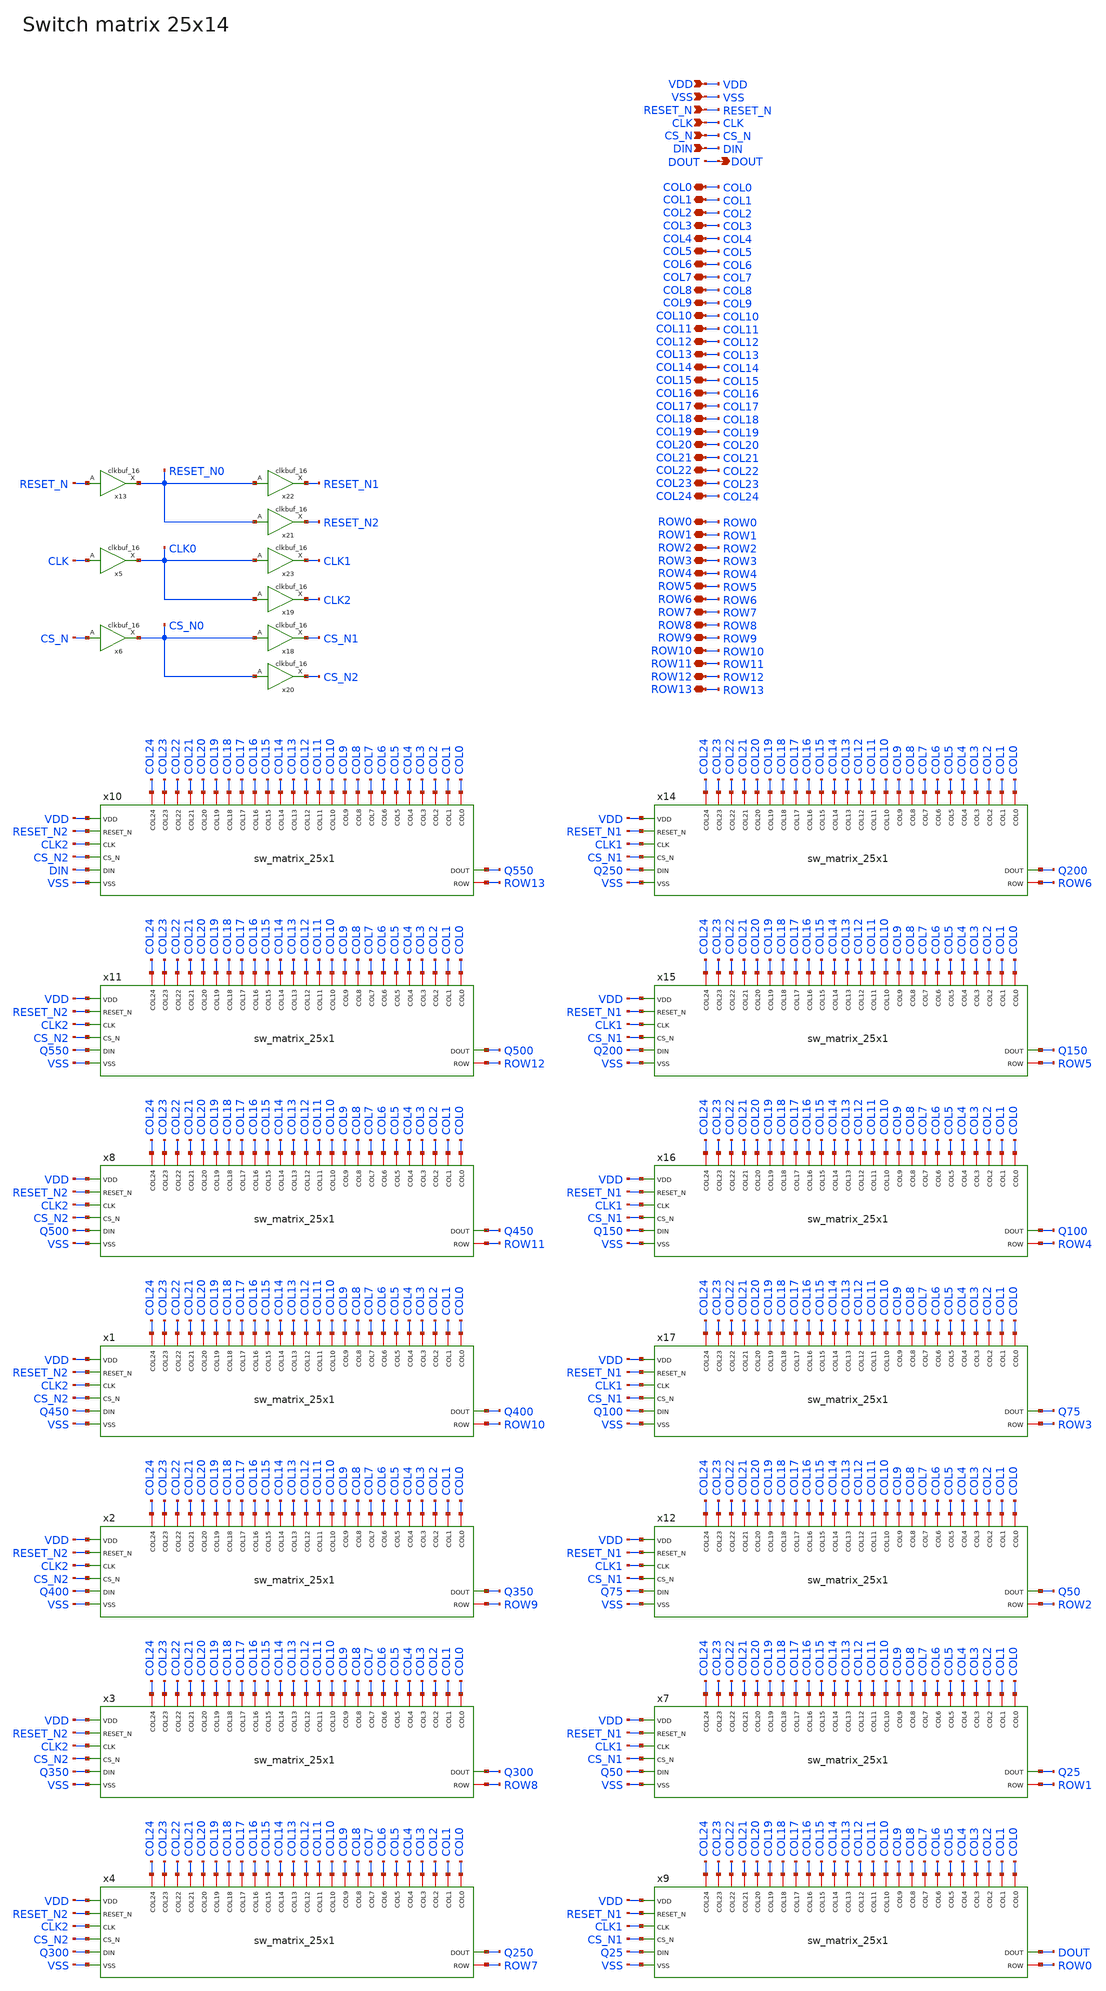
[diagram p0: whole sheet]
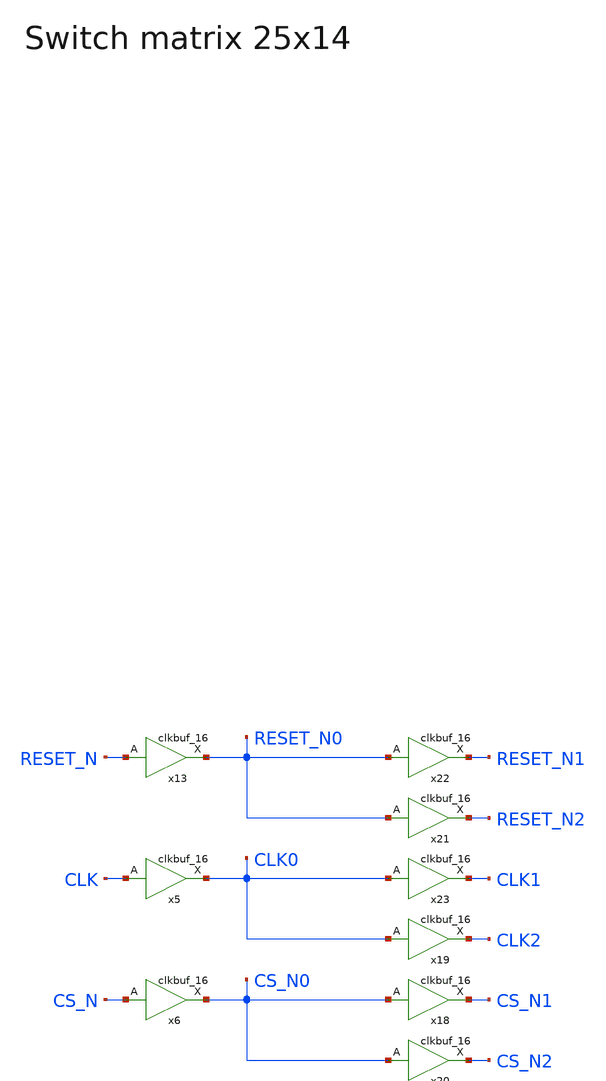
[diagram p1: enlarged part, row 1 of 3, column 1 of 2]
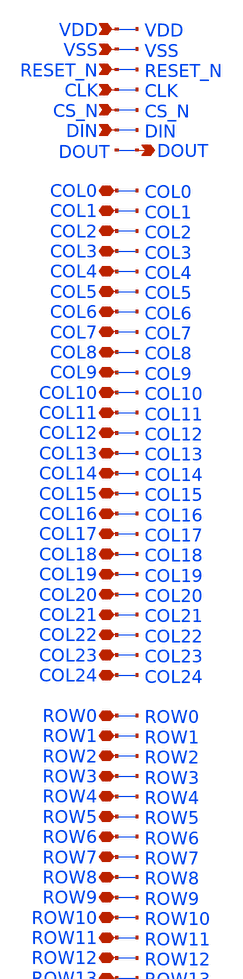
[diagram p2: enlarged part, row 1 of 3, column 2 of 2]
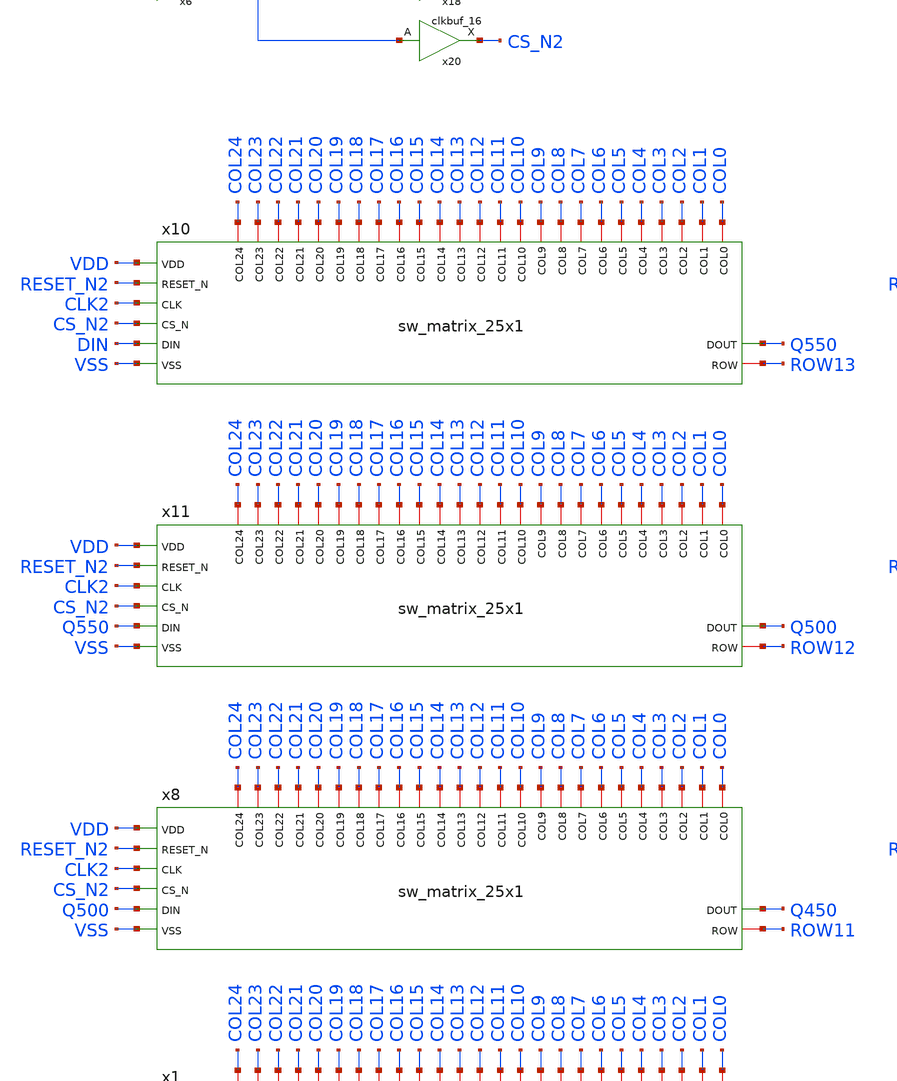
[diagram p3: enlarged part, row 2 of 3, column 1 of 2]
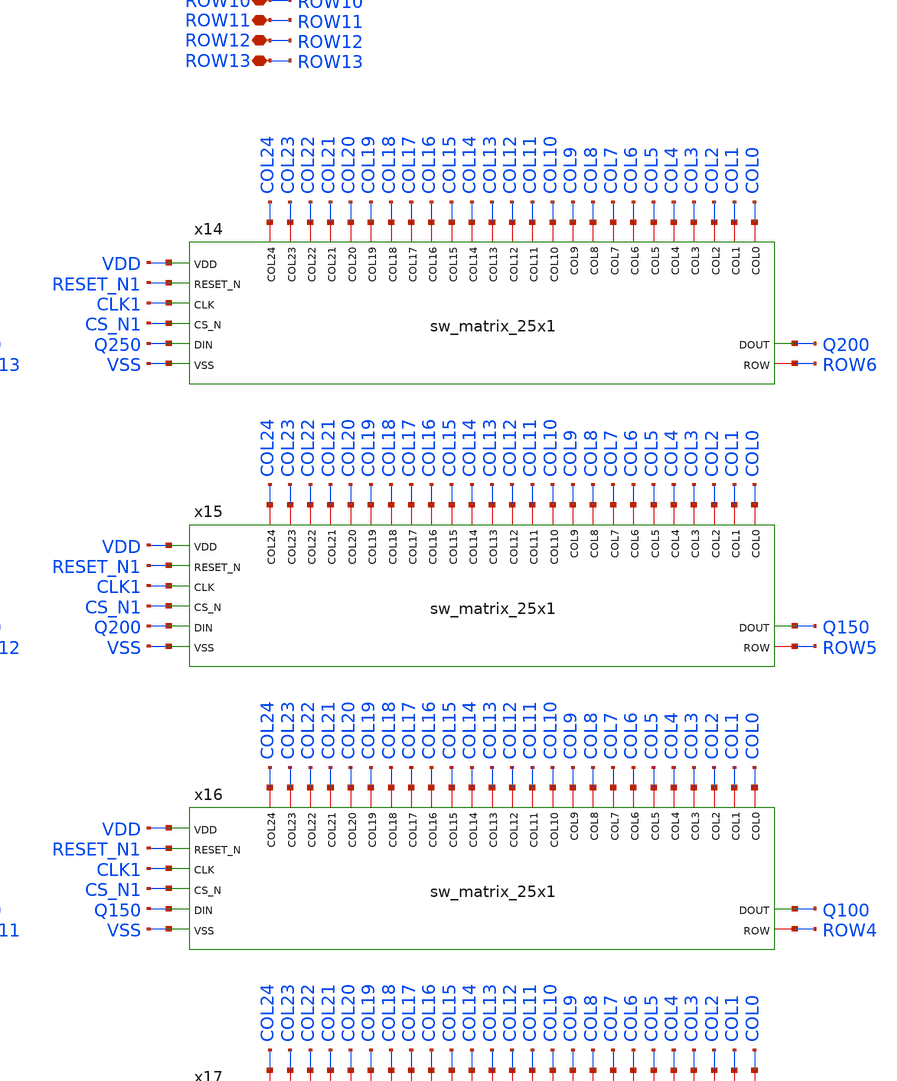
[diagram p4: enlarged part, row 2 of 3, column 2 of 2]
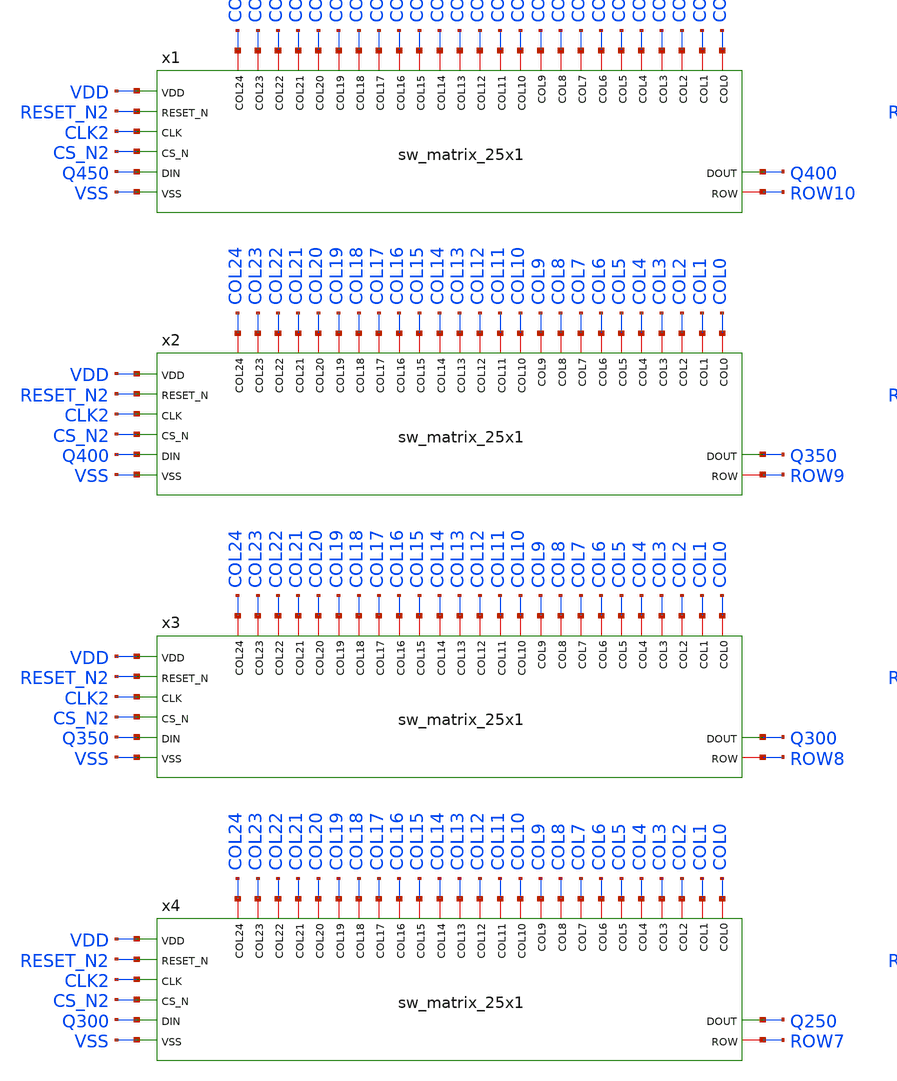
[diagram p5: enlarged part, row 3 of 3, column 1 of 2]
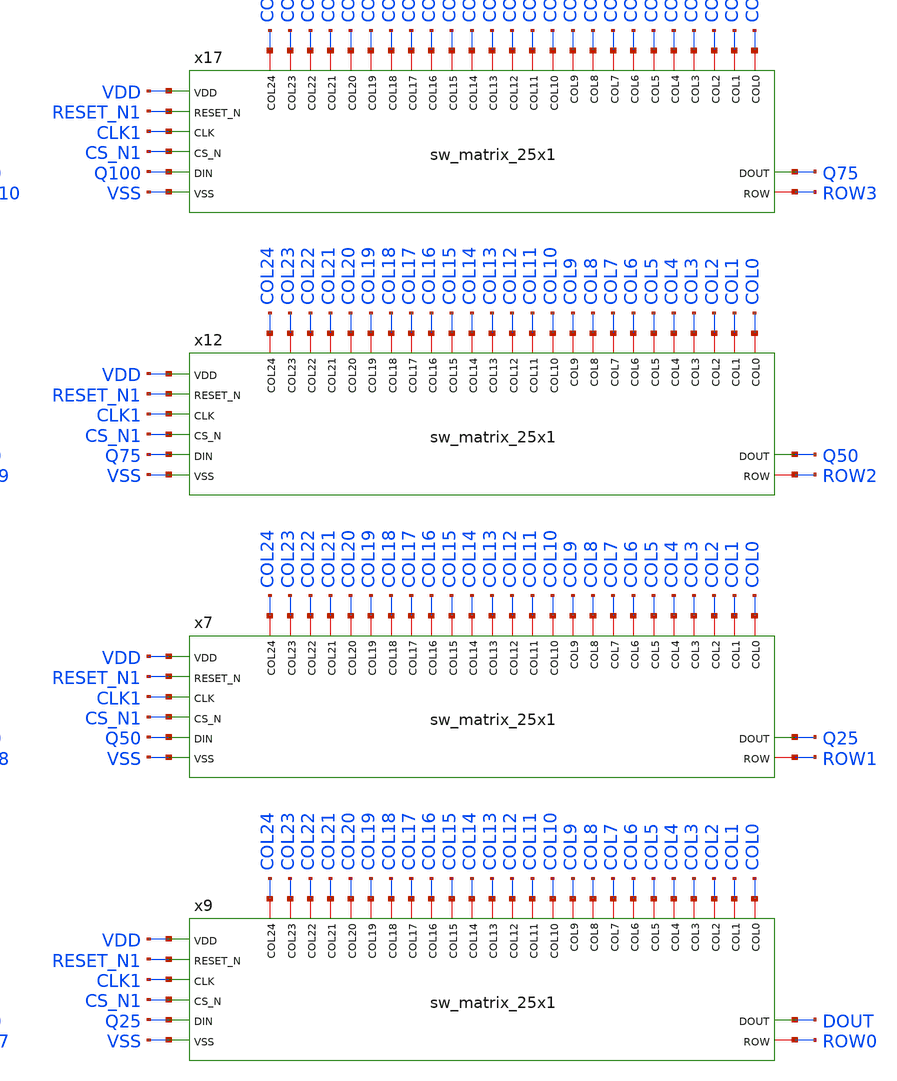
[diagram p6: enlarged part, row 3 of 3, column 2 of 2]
** sch_path: designs/libs/core_analog/sw_matrix/sw_matrix_25x14.sch
* Copyright 2022 GlobalFoundries PDK Authors
* Licensed under the Apache License, Version 2.0 (the "License");
* you may not use this file except in compliance with the License.
* You may obtain a copy of the License at
* https://www.apache.org/licenses/LICENSE-2.0
* Unless required by applicable law or agreed to in writing, software
* distributed under the License is distributed on an "AS IS" BASIS,
* WITHOUT WARRANTIES OR CONDITIONS OF ANY KIND, either express or implied.
* See the License for the specific language governing permissions and
* limitations under the License.
**.subckt sw_matrix_25x14 VDD VSS RESET_N CLK CS_N DIN COL0 COL1 COL2 COL3 COL4 ROW0 DOUT COL5 COL6
*+ COL7 COL8 COL9 COL10 COL11 COL12 COL13 COL14 COL15 COL16 COL17 COL18 COL19 COL20 COL21 COL22 COL23 COL24
*+ ROW1 ROW2 ROW3 ROW4 ROW5 ROW6 ROW7 ROW8 ROW9 ROW10 ROW11 ROW12 ROW13
*.ipin VDD
*.ipin VSS
*.ipin RESET_N
*.ipin CLK
*.ipin CS_N
*.ipin DIN
*.iopin COL0
*.iopin COL1
*.iopin COL2
*.iopin COL3
*.iopin COL4
*.iopin ROW0
*.opin DOUT
*.iopin COL5
*.iopin COL6
*.iopin COL7
*.iopin COL8
*.iopin COL9
*.iopin COL10
*.iopin COL11
*.iopin COL12
*.iopin COL13
*.iopin COL14
*.iopin COL15
*.iopin COL16
*.iopin COL17
*.iopin COL18
*.iopin COL19
*.iopin COL20
*.iopin COL21
*.iopin COL22
*.iopin COL23
*.iopin COL24
*.iopin ROW1
*.iopin ROW2
*.iopin ROW3
*.iopin ROW4
*.iopin ROW5
*.iopin ROW6
*.iopin ROW7
*.iopin ROW8
*.iopin ROW9
*.iopin ROW10
*.iopin ROW11
*.iopin ROW12
*.iopin ROW13
x5 CLK CLK0 VDD VDD VSS VSS gf180mcu_fd_sc_mcu7t5v0__clkbuf_16
x13 RESET_N RESET_N0 VDD VDD VSS VSS gf180mcu_fd_sc_mcu7t5v0__clkbuf_16
x6 CS_N CS_N0 VDD VDD VSS VSS gf180mcu_fd_sc_mcu7t5v0__clkbuf_16
x8 COL15 COL0 COL20 COL5 COL10 VDD COL6 VSS COL11 COL1 COL21 COL16 COL22 COL2 COL17 COL12 RESET_N2
+ COL7 COL18 COL3 COL13 CLK2 COL8 COL23 COL19 CS_N2 COL14 COL24 COL9 COL4 Q500 Q450 ROW11 sw_matrix_25x1
x1 COL15 COL0 COL20 COL5 COL10 VDD COL6 VSS COL11 COL1 COL21 COL16 COL22 COL2 COL17 COL12 RESET_N2
+ COL7 COL18 COL3 COL13 CLK2 COL8 COL23 COL19 CS_N2 COL14 COL24 COL9 COL4 Q450 Q400 ROW10 sw_matrix_25x1
x2 COL15 COL0 COL20 COL5 COL10 VDD COL6 VSS COL11 COL1 COL21 COL16 COL22 COL2 COL17 COL12 RESET_N2
+ COL7 COL18 COL3 COL13 CLK2 COL8 COL23 COL19 CS_N2 COL14 COL24 COL9 COL4 Q400 Q350 ROW9 sw_matrix_25x1
x3 COL15 COL0 COL20 COL5 COL10 VDD COL6 VSS COL11 COL1 COL21 COL16 COL22 COL2 COL17 COL12 RESET_N2
+ COL7 COL18 COL3 COL13 CLK2 COL8 COL23 COL19 CS_N2 COL14 COL24 COL9 COL4 Q350 Q300 ROW8 sw_matrix_25x1
x4 COL15 COL0 COL20 COL5 COL10 VDD COL6 VSS COL11 COL1 COL21 COL16 COL22 COL2 COL17 COL12 RESET_N2
+ COL7 COL18 COL3 COL13 CLK2 COL8 COL23 COL19 CS_N2 COL14 COL24 COL9 COL4 Q300 Q250 ROW7 sw_matrix_25x1
x7 COL15 COL0 COL20 COL5 COL10 VDD COL6 VSS COL11 COL1 COL21 COL16 COL22 COL2 COL17 COL12 RESET_N1
+ COL7 COL18 COL3 COL13 CLK1 COL8 COL23 COL19 CS_N1 COL14 COL24 COL9 COL4 Q50 Q25 ROW1 sw_matrix_25x1
x9 COL15 COL0 COL20 COL5 COL10 VDD COL6 VSS COL11 COL1 COL21 COL16 COL22 COL2 COL17 COL12 RESET_N1
+ COL7 COL18 COL3 COL13 CLK1 COL8 COL23 COL19 CS_N1 COL14 COL24 COL9 COL4 Q25 DOUT ROW0 sw_matrix_25x1
x10 COL15 COL0 COL20 COL5 COL10 VDD COL6 VSS COL11 COL1 COL21 COL16 COL22 COL2 COL17 COL12 RESET_N2
+ COL7 COL18 COL3 COL13 CLK2 COL8 COL23 COL19 CS_N2 COL14 COL24 COL9 COL4 DIN Q550 ROW13 sw_matrix_25x1
x11 COL15 COL0 COL20 COL5 COL10 VDD COL6 VSS COL11 COL1 COL21 COL16 COL22 COL2 COL17 COL12 RESET_N2
+ COL7 COL18 COL3 COL13 CLK2 COL8 COL23 COL19 CS_N2 COL14 COL24 COL9 COL4 Q550 Q500 ROW12 sw_matrix_25x1
x12 COL15 COL0 COL20 COL5 COL10 VDD COL6 VSS COL11 COL1 COL21 COL16 COL22 COL2 COL17 COL12 RESET_N1
+ COL7 COL18 COL3 COL13 CLK1 COL8 COL23 COL19 CS_N1 COL14 COL24 COL9 COL4 Q75 Q50 ROW2 sw_matrix_25x1
x14 COL15 COL0 COL20 COL5 COL10 VDD COL6 VSS COL11 COL1 COL21 COL16 COL22 COL2 COL17 COL12 RESET_N1
+ COL7 COL18 COL3 COL13 CLK1 COL8 COL23 COL19 CS_N1 COL14 COL24 COL9 COL4 Q250 Q200 ROW6 sw_matrix_25x1
x15 COL15 COL0 COL20 COL5 COL10 VDD COL6 VSS COL11 COL1 COL21 COL16 COL22 COL2 COL17 COL12 RESET_N1
+ COL7 COL18 COL3 COL13 CLK1 COL8 COL23 COL19 CS_N1 COL14 COL24 COL9 COL4 Q200 Q150 ROW5 sw_matrix_25x1
x16 COL15 COL0 COL20 COL5 COL10 VDD COL6 VSS COL11 COL1 COL21 COL16 COL22 COL2 COL17 COL12 RESET_N1
+ COL7 COL18 COL3 COL13 CLK1 COL8 COL23 COL19 CS_N1 COL14 COL24 COL9 COL4 Q150 Q100 ROW4 sw_matrix_25x1
x17 COL15 COL0 COL20 COL5 COL10 VDD COL6 VSS COL11 COL1 COL21 COL16 COL22 COL2 COL17 COL12 RESET_N1
+ COL7 COL18 COL3 COL13 CLK1 COL8 COL23 COL19 CS_N1 COL14 COL24 COL9 COL4 Q100 Q75 ROW3 sw_matrix_25x1
x18 CS_N0 CS_N1 VDD VDD VSS VSS gf180mcu_fd_sc_mcu7t5v0__clkbuf_16
x19 CLK0 CLK2 VDD VDD VSS VSS gf180mcu_fd_sc_mcu7t5v0__clkbuf_16
x20 CS_N0 CS_N2 VDD VDD VSS VSS gf180mcu_fd_sc_mcu7t5v0__clkbuf_16
x21 RESET_N0 RESET_N2 VDD VDD VSS VSS gf180mcu_fd_sc_mcu7t5v0__clkbuf_16
x22 RESET_N0 RESET_N1 VDD VDD VSS VSS gf180mcu_fd_sc_mcu7t5v0__clkbuf_16
x23 CLK0 CLK1 VDD VDD VSS VSS gf180mcu_fd_sc_mcu7t5v0__clkbuf_16
**** begin user architecture code

.include /foss/pdks/gf180mcuD/libs.ref/gf180mcu_fd_sc_mcu7t5v0/spice/gf180mcu_fd_sc_mcu7t5v0.spice


**** end user architecture code
**.ends
.end
